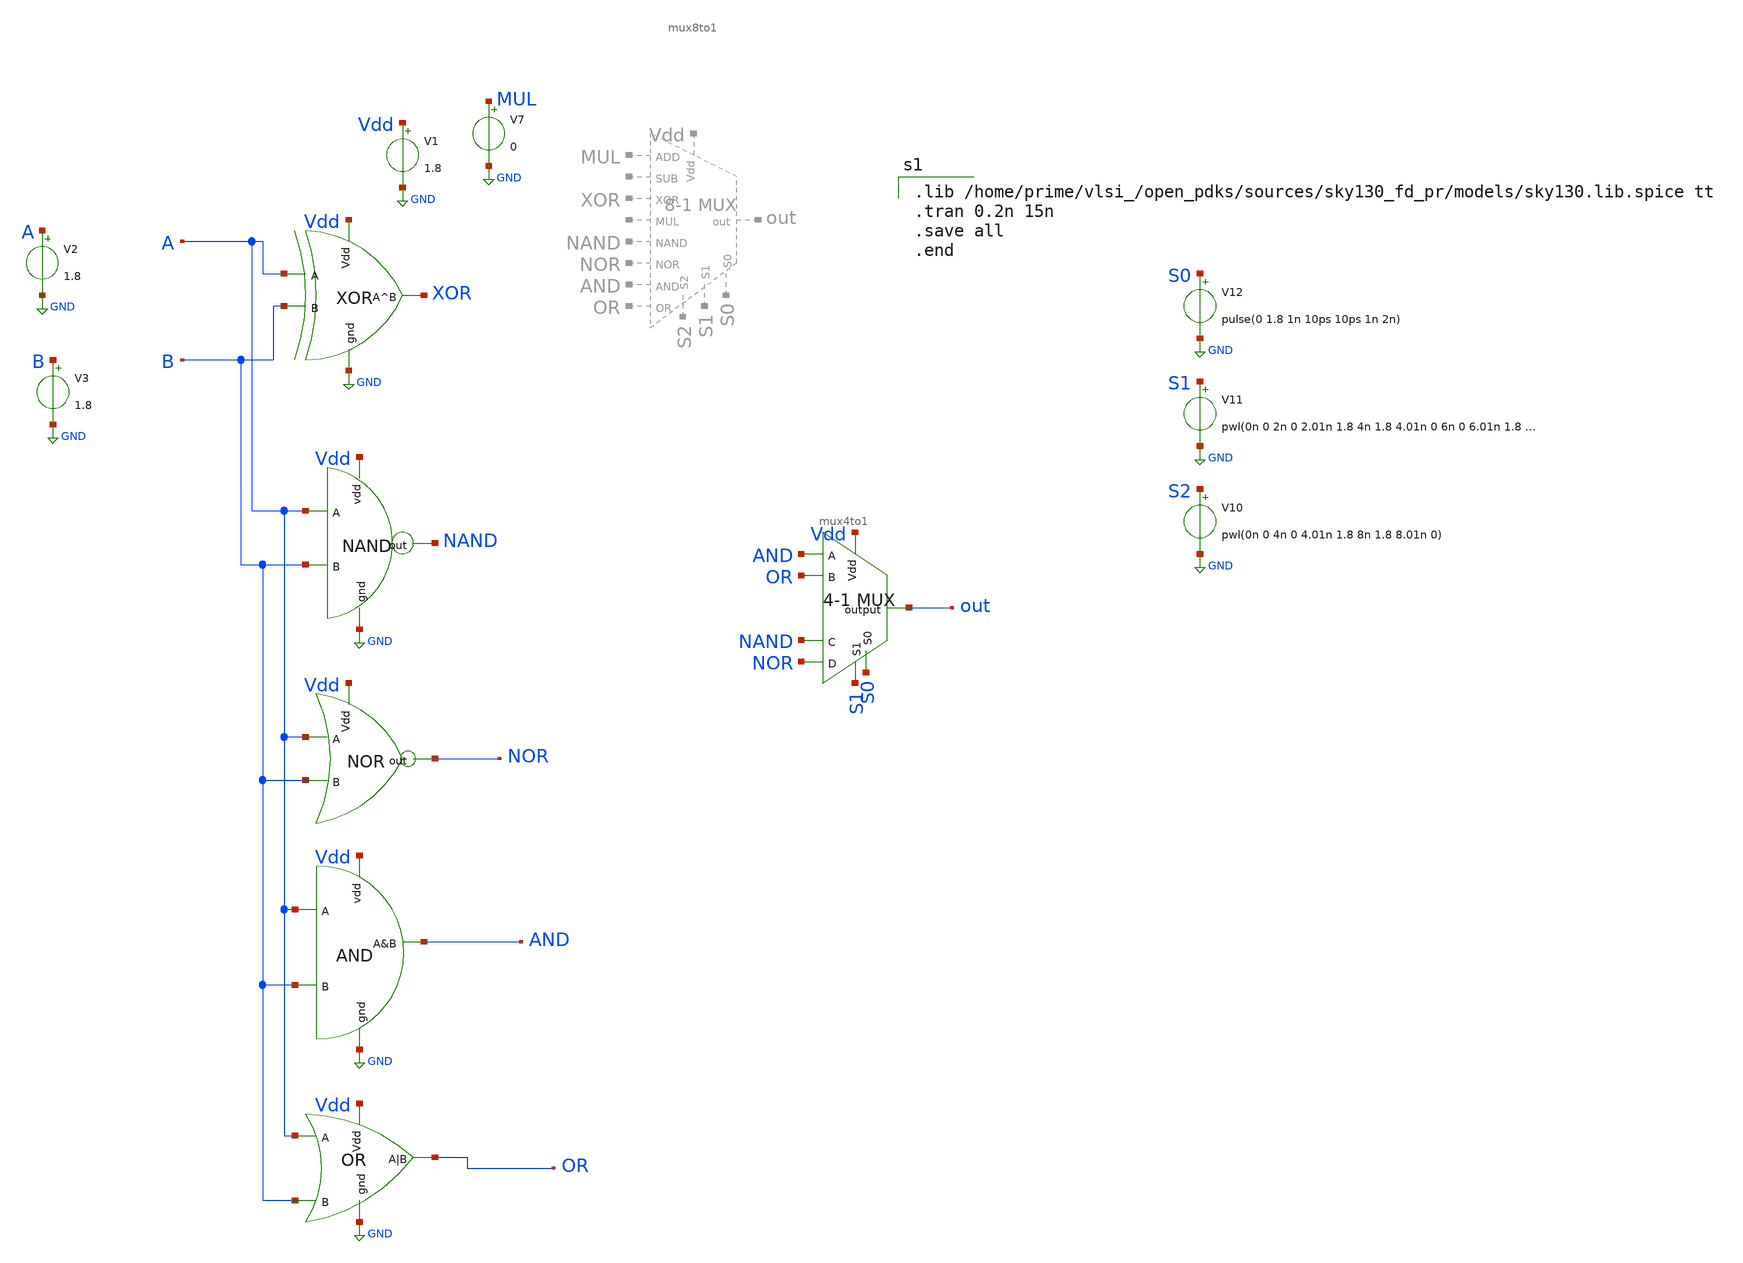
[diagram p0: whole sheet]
** sch_path: extra_stuff/new_sandbox.sch
**.subckt new_sandbox
V1 Vdd GND 1.8
V2 A GND 1.8
V3 B GND 1.8
x2 Vdd GND XOR A B xor
x3 NAND Vdd A B GND NAND
x4 NOR Vdd A B nor
x5 A B AND Vdd GND and
x6 Vdd GND OR A B or
V10 S2 GND pwl(0n 0 4n 0 4.01n 1.8 8n 1.8 8.01n 0)
V11 S1 GND pwl(0n 0 2n 0 2.01n 1.8 4n 1.8 4.01n 0 6n 0 6.01n 1.8 8n 1.8 8.01n 0)
V12 S0 GND pulse(0 1.8 1n 10ps 10ps 1n 2n)
V7 MUL GND 0
x7 out AND OR NAND NOR Vdd S0 S1 mux4to1
**** begin user architecture code

.lib /home/prime/vlsi_/open_pdks/sources/sky130_fd_pr/models/sky130.lib.spice tt
.tran 0.2n 15n
.save all
.end

**** end user architecture code
**.ends
.GLOBAL GND
.end
